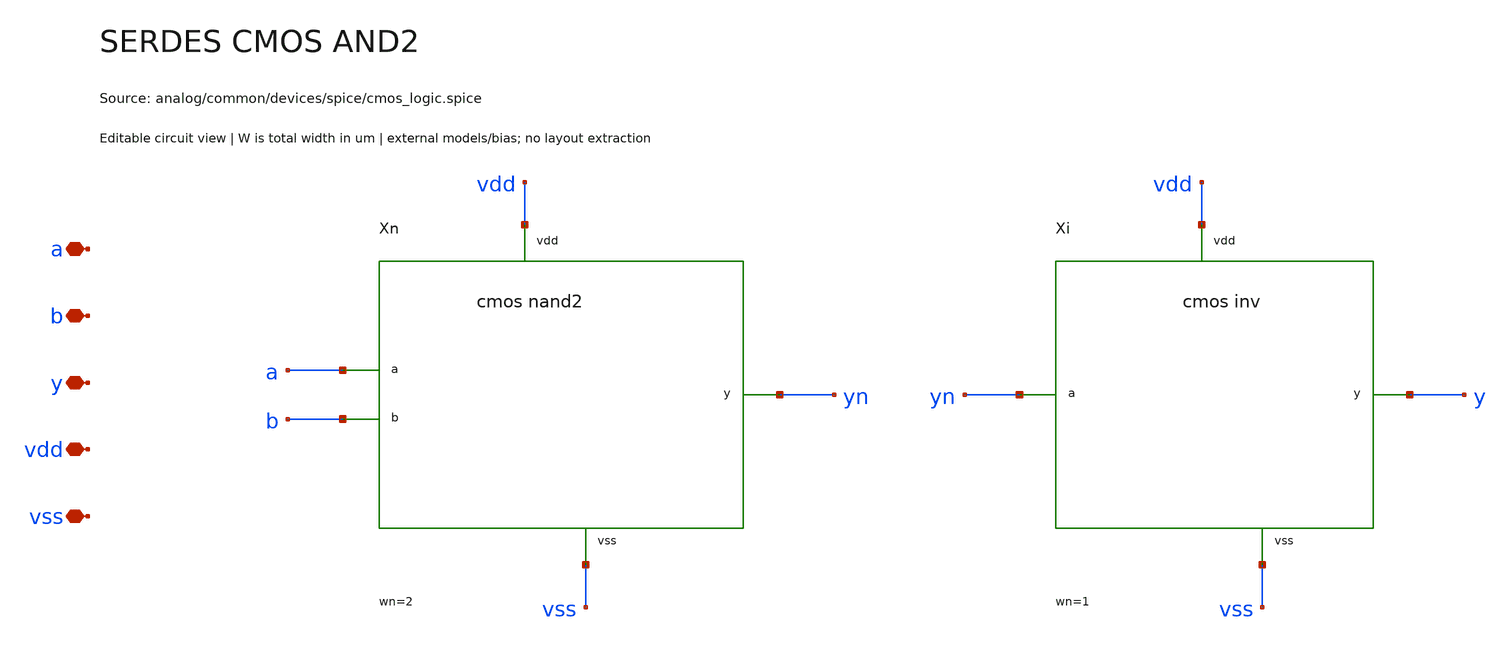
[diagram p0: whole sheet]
** sch_path: analog/common/devices/schematic/serdes_cmos_and2.sch
**.subckt serdes_cmos_and2 a b y vdd vss
*.iopin a
*.iopin b
*.iopin y
*.iopin vdd
*.iopin vss
Xn a b yn vdd vss serdes_cmos_nand2 wn=2 wp=2
Xi yn y vdd vss serdes_cmos_inv wn=1 wp=2
**.ends

* expanding   symbol:  serdes/serdes_cmos_nand2.sym # of pins=5
** sym_path: analog/common/devices/schematic/serdes_cmos_nand2.sym
** sch_path: analog/common/devices/schematic/serdes_cmos_nand2.sch
.subckt serdes_cmos_nand2 a b y vdd vss  wn=2 wp=2
*.iopin a
*.iopin b
*.iopin y
*.iopin vdd
*.iopin vss
Xna y a mid vss serdes_nfet w={wn} l=0.15 nf=1
Xnb mid b vss vss serdes_nfet w={wn} l=0.15 nf=1
Xpa y a vdd vdd serdes_pfet w={wp} l=0.15 nf=1
Xpb y b vdd vdd serdes_pfet w={wp} l=0.15 nf=1
.ends


* expanding   symbol:  serdes/serdes_cmos_inv.sym # of pins=4
** sym_path: analog/common/devices/schematic/serdes_cmos_inv.sym
** sch_path: analog/common/devices/schematic/serdes_cmos_inv.sch
.subckt serdes_cmos_inv a y vdd vss  wn=1 wp=2
*.iopin a
*.iopin y
*.iopin vdd
*.iopin vss
Xn y a vss vss serdes_nfet w={wn} l=0.15 nf=1
Xp y a vdd vdd serdes_pfet w={wp} l=0.15 nf=1
.ends


* expanding   symbol:  serdes/serdes_nfet.sym # of pins=4
** sym_path: analog/common/devices/schematic/serdes_nfet.sym
** sch_path: analog/common/devices/schematic/serdes_nfet.sch
.subckt serdes_nfet d g s b  w=1 l=0.15 nf=1
*.iopin d
*.iopin g
*.iopin s
*.iopin b
Xmos d g s b sky130_fd_pr__nfet_01v8 w={w} l={l} nf={nf} ad={floor((nf+1)/2)*(w/nf)*0.29} as={floor((nf+2)/2)*(w/nf)*0.29}
+ pd={2*floor((nf+1)/2)*(w/nf+0.29)} ps={2*floor((nf+2)/2)*(w/nf+0.29)}
.ends


* expanding   symbol:  serdes/serdes_pfet.sym # of pins=4
** sym_path: analog/common/devices/schematic/serdes_pfet.sym
** sch_path: analog/common/devices/schematic/serdes_pfet.sch
.subckt serdes_pfet d g s b  w=3 l=0.15 nf=1
*.iopin d
*.iopin g
*.iopin s
*.iopin b
Xmos d g s b sky130_fd_pr__pfet_01v8 w={w} l={l} nf={nf} ad={floor((nf+1)/2)*(w/nf)*0.29} as={floor((nf+2)/2)*(w/nf)*0.29}
+ pd={2*floor((nf+1)/2)*(w/nf+0.29)} ps={2*floor((nf+2)/2)*(w/nf+0.29)}
.ends

.end
